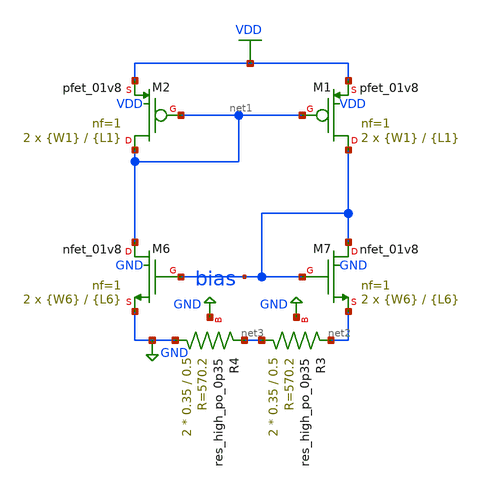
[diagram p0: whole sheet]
** sch_path: xschem/untitled-1.sch
**.subckt untitled-1
XM1 bias net1 VDD VDD sky130_fd_pr__pfet_01v8 L={L1} W={W1} nf=1 ad='int((nf+1)/2) * W/nf * 0.29' as='int((nf+2)/2) * W/nf * 0.29'
+ pd='2*int((nf+1)/2) * (W/nf + 0.29)' ps='2*int((nf+2)/2) * (W/nf + 0.29)' nrd='0.29 / W' nrs='0.29 / W'
+ sa=0 sb=0 sd=0 mult=2 m=2
XM2 net1 net1 VDD VDD sky130_fd_pr__pfet_01v8 L={L1} W={W1} nf=1 ad='int((nf+1)/2) * W/nf * 0.29' as='int((nf+2)/2) * W/nf * 0.29'
+ pd='2*int((nf+1)/2) * (W/nf + 0.29)' ps='2*int((nf+2)/2) * (W/nf + 0.29)' nrd='0.29 / W' nrs='0.29 / W'
+ sa=0 sb=0 sd=0 mult=2 m=2
XM6 net1 bias GND GND sky130_fd_pr__nfet_01v8 L={L6} W={W6} nf=1 ad='int((nf+1)/2) * W/nf * 0.29' as='int((nf+2)/2) * W/nf * 0.29'
+ pd='2*int((nf+1)/2) * (W/nf + 0.29)' ps='2*int((nf+2)/2) * (W/nf + 0.29)' nrd='0.29 / W' nrs='0.29 / W'
+ sa=0 sb=0 sd=0 mult=2 m=2
XM7 bias bias net2 GND sky130_fd_pr__nfet_01v8 L={L6} W={W6} nf=1 ad='int((nf+1)/2) * W/nf * 0.29' as='int((nf+2)/2) * W/nf * 0.29'
+ pd='2*int((nf+1)/2) * (W/nf + 0.29)' ps='2*int((nf+2)/2) * (W/nf + 0.29)' nrd='0.29 / W' nrs='0.29 / W'
+ sa=0 sb=0 sd=0 mult=2 m=2
XR3 net3 net2 GND sky130_fd_pr__res_high_po_0p35 L=0.5 mult=2 m=2
XR4 GND net3 GND sky130_fd_pr__res_high_po_0p35 L=0.5 mult=2 m=2
**.ends
.GLOBAL GND
.GLOBAL VDD
.end
